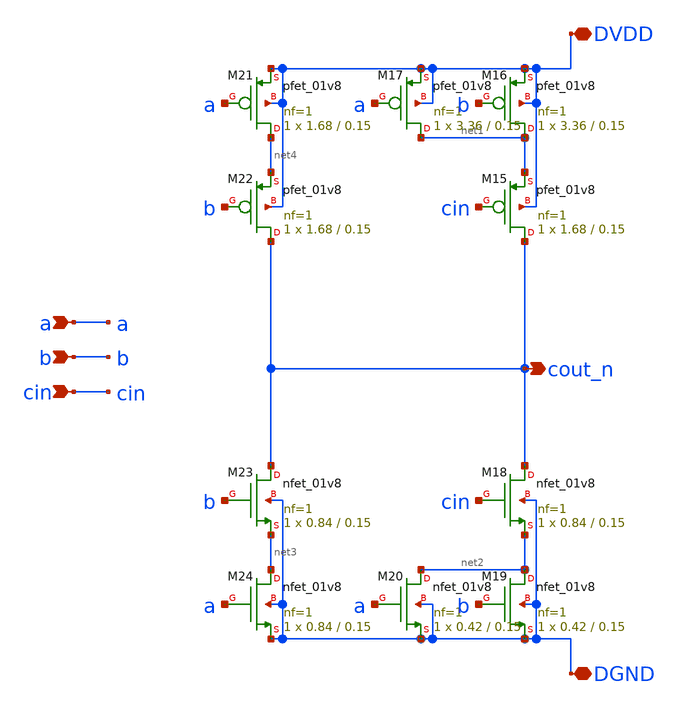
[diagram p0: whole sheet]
** sch_path: tut6/incr/carry/fa.sch
**.subckt fa a b cin DGND DVDD cout_n
*.ipin a
*.ipin b
*.ipin cin
*.iopin DGND
*.iopin DVDD
*.opin cout_n
XM15 cout_n cin net1 DVDD sky130_fd_pr__pfet_01v8 L=0.15 W=1.68 nf=1 ad='int((nf+1)/2) * W/nf * 0.29'
+ as='int((nf+2)/2) * W/nf * 0.29' pd='2*int((nf+1)/2) * (W/nf + 0.29)' ps='2*int((nf+2)/2) * (W/nf + 0.29)'
+ nrd='0.29 / W' nrs='0.29 / W' sa=0 sb=0 sd=0 mult=1 m=1
XM16 net1 b DVDD DVDD sky130_fd_pr__pfet_01v8 L=0.15 W=3.36 nf=1 ad='int((nf+1)/2) * W/nf * 0.29' as='int((nf+2)/2) * W/nf * 0.29'
+ pd='2*int((nf+1)/2) * (W/nf + 0.29)' ps='2*int((nf+2)/2) * (W/nf + 0.29)' nrd='0.29 / W' nrs='0.29 / W'
+ sa=0 sb=0 sd=0 mult=1 m=1
XM17 net1 a DVDD DVDD sky130_fd_pr__pfet_01v8 L=0.15 W=3.36 nf=1 ad='int((nf+1)/2) * W/nf * 0.29' as='int((nf+2)/2) * W/nf * 0.29'
+ pd='2*int((nf+1)/2) * (W/nf + 0.29)' ps='2*int((nf+2)/2) * (W/nf + 0.29)' nrd='0.29 / W' nrs='0.29 / W'
+ sa=0 sb=0 sd=0 mult=1 m=1
XM18 cout_n cin net2 DGND sky130_fd_pr__nfet_01v8 L=0.15 W=0.84 nf=1 ad='int((nf+1)/2) * W/nf * 0.29'
+ as='int((nf+2)/2) * W/nf * 0.29' pd='2*int((nf+1)/2) * (W/nf + 0.29)' ps='2*int((nf+2)/2) * (W/nf + 0.29)'
+ nrd='0.29 / W' nrs='0.29 / W' sa=0 sb=0 sd=0 mult=1 m=1
XM19 net2 b DGND DGND sky130_fd_pr__nfet_01v8 L=0.15 W=0.42 nf=1 ad='int((nf+1)/2) * W/nf * 0.29' as='int((nf+2)/2) * W/nf * 0.29'
+ pd='2*int((nf+1)/2) * (W/nf + 0.29)' ps='2*int((nf+2)/2) * (W/nf + 0.29)' nrd='0.29 / W' nrs='0.29 / W'
+ sa=0 sb=0 sd=0 mult=1 m=1
XM20 net2 a DGND DGND sky130_fd_pr__nfet_01v8 L=0.15 W=0.42 nf=1 ad='int((nf+1)/2) * W/nf * 0.29' as='int((nf+2)/2) * W/nf * 0.29'
+ pd='2*int((nf+1)/2) * (W/nf + 0.29)' ps='2*int((nf+2)/2) * (W/nf + 0.29)' nrd='0.29 / W' nrs='0.29 / W'
+ sa=0 sb=0 sd=0 mult=1 m=1
XM21 net4 a DVDD DVDD sky130_fd_pr__pfet_01v8 L=0.15 W=1.68 nf=1 ad='int((nf+1)/2) * W/nf * 0.29' as='int((nf+2)/2) * W/nf * 0.29'
+ pd='2*int((nf+1)/2) * (W/nf + 0.29)' ps='2*int((nf+2)/2) * (W/nf + 0.29)' nrd='0.29 / W' nrs='0.29 / W'
+ sa=0 sb=0 sd=0 mult=1 m=1
XM22 cout_n b net4 DVDD sky130_fd_pr__pfet_01v8 L=0.15 W=1.68 nf=1 ad='int((nf+1)/2) * W/nf * 0.29' as='int((nf+2)/2) * W/nf * 0.29'
+ pd='2*int((nf+1)/2) * (W/nf + 0.29)' ps='2*int((nf+2)/2) * (W/nf + 0.29)' nrd='0.29 / W' nrs='0.29 / W'
+ sa=0 sb=0 sd=0 mult=1 m=1
XM23 cout_n b net3 DGND sky130_fd_pr__nfet_01v8 L=0.15 W=0.84 nf=1 ad='int((nf+1)/2) * W/nf * 0.29' as='int((nf+2)/2) * W/nf * 0.29'
+ pd='2*int((nf+1)/2) * (W/nf + 0.29)' ps='2*int((nf+2)/2) * (W/nf + 0.29)' nrd='0.29 / W' nrs='0.29 / W'
+ sa=0 sb=0 sd=0 mult=1 m=1
XM24 net3 a DGND DGND sky130_fd_pr__nfet_01v8 L=0.15 W=0.84 nf=1 ad='int((nf+1)/2) * W/nf * 0.29' as='int((nf+2)/2) * W/nf * 0.29'
+ pd='2*int((nf+1)/2) * (W/nf + 0.29)' ps='2*int((nf+2)/2) * (W/nf + 0.29)' nrd='0.29 / W' nrs='0.29 / W'
+ sa=0 sb=0 sd=0 mult=1 m=1
**.ends
.end
